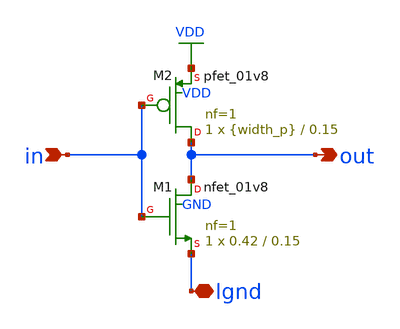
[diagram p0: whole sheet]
** sch_path: tutorial_4/inv_amm.sch
**.subckt inv_amm in out lgnd
*.ipin in
*.opin out
*.iopin lgnd
XM1 out in lgnd GND sky130_fd_pr__nfet_01v8 L=0.15 W=0.42 nf=1 ad='int((nf+1)/2) * W/nf * 0.29' as='int((nf+2)/2) * W/nf * 0.29'
+ pd='2*int((nf+1)/2) * (W/nf + 0.29)' ps='2*int((nf+2)/2) * (W/nf + 0.29)' nrd='0.29 / W' nrs='0.29 / W'
+ sa=0 sb=0 sd=0 mult=1 m=1
XM2 out in VDD VDD sky130_fd_pr__pfet_01v8 L=0.15 W={width_p} nf=1 ad='int((nf+1)/2) * W/nf * 0.29' as='int((nf+2)/2) * W/nf * 0.29'
+ pd='2*int((nf+1)/2) * (W/nf + 0.29)' ps='2*int((nf+2)/2) * (W/nf + 0.29)' nrd='0.29 / W' nrs='0.29 / W'
+ sa=0 sb=0 sd=0 mult=1 m=1
**.ends
.GLOBAL VDD
.end
